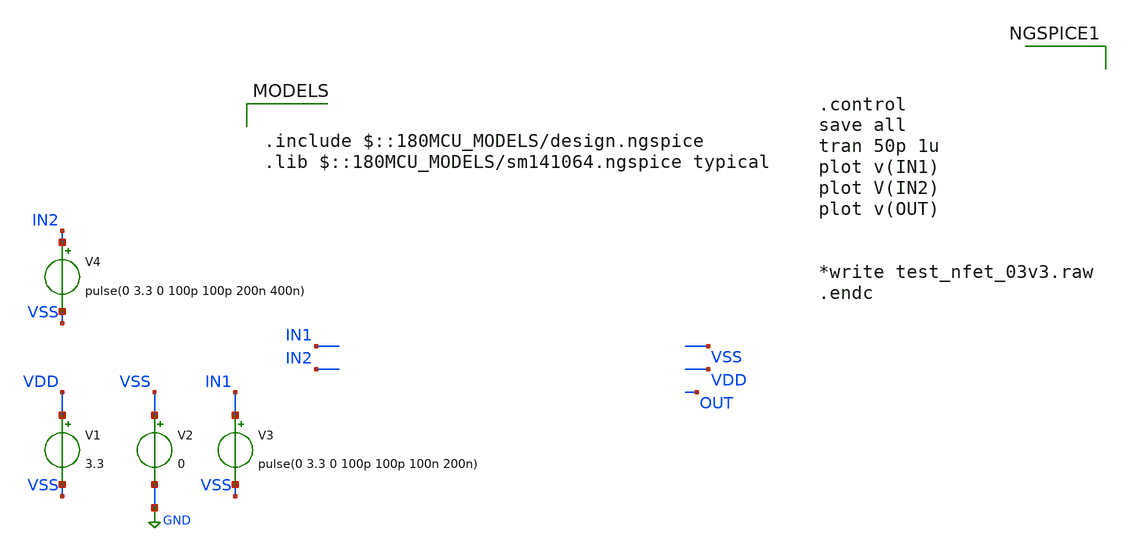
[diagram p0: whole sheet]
** sch_path: Clock_Generator_PAKISTAN_02/Schematics/pex_and2_test.sch
**.subckt pex_and2_test
V1 VDD VSS 3.3
V2 VSS GND 0
V3 IN1 VSS pulse(0 3.3 0 100p 100p 100n 200n)
V4 IN2 VSS pulse(0 3.3 0 100p 100p 200n 400n)
**** begin user architecture code

.include $::180MCU_MODELS/design.ngspice
.lib $::180MCU_MODELS/sm141064.ngspice typical




.control
save all
tran 50p 1u
plot v(IN1)
plot V(IN2)
plot v(OUT)


*write test_nfet_03v3.raw
.endc


**** end user architecture code
**.ends
.GLOBAL GND
.end
